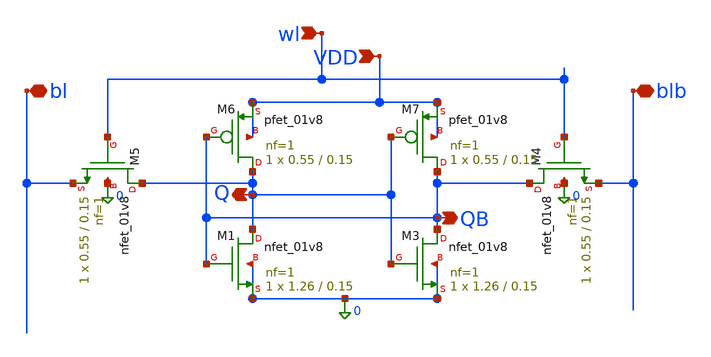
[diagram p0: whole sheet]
** sch_path: xschem/Subcircuits/six_t.sch
**.subckt six_t bl Q QB wl VDD blb
*.iopin bl
*.opin Q
*.opin QB
*.ipin wl
*.ipin VDD
*.iopin blb
XM3 QB Q 0 0 sky130_fd_pr__nfet_01v8 L=0.15 W=1.26 nf=1 ad='int((nf+1)/2) * W/nf * 0.29' as='int((nf+2)/2) * W/nf * 0.29'
+ pd='2*int((nf+1)/2) * (W/nf + 0.29)' ps='2*int((nf+2)/2) * (W/nf + 0.29)' nrd='0.29 / W' nrs='0.29 / W'
+ sa=0 sb=0 sd=0 mult=1 m=1
XM4 QB wl blb 0 sky130_fd_pr__nfet_01v8 L=0.15 W=0.55 nf=1 ad='int((nf+1)/2) * W/nf * 0.29' as='int((nf+2)/2) * W/nf * 0.29'
+ pd='2*int((nf+1)/2) * (W/nf + 0.29)' ps='2*int((nf+2)/2) * (W/nf + 0.29)' nrd='0.29 / W' nrs='0.29 / W'
+ sa=0 sb=0 sd=0 mult=1 m=1
XM5 Q wl bl 0 sky130_fd_pr__nfet_01v8 L=0.15 W=0.55 nf=1 ad='int((nf+1)/2) * W/nf * 0.29' as='int((nf+2)/2) * W/nf * 0.29'
+ pd='2*int((nf+1)/2) * (W/nf + 0.29)' ps='2*int((nf+2)/2) * (W/nf + 0.29)' nrd='0.29 / W' nrs='0.29 / W'
+ sa=0 sb=0 sd=0 mult=1 m=1
XM6 Q QB VDD VDD sky130_fd_pr__pfet_01v8 L=0.15 W=0.55 nf=1 ad='int((nf+1)/2) * W/nf * 0.29' as='int((nf+2)/2) * W/nf * 0.29'
+ pd='2*int((nf+1)/2) * (W/nf + 0.29)' ps='2*int((nf+2)/2) * (W/nf + 0.29)' nrd='0.29 / W' nrs='0.29 / W'
+ sa=0 sb=0 sd=0 mult=1 m=1
XM7 QB Q VDD VDD sky130_fd_pr__pfet_01v8 L=0.15 W=0.55 nf=1 ad='int((nf+1)/2) * W/nf * 0.29' as='int((nf+2)/2) * W/nf * 0.29'
+ pd='2*int((nf+1)/2) * (W/nf + 0.29)' ps='2*int((nf+2)/2) * (W/nf + 0.29)' nrd='0.29 / W' nrs='0.29 / W'
+ sa=0 sb=0 sd=0 mult=1 m=1
XM1 Q QB 0 0 sky130_fd_pr__nfet_01v8 L=0.15 W=1.26 nf=1 ad='int((nf+1)/2) * W/nf * 0.29' as='int((nf+2)/2) * W/nf * 0.29'
+ pd='2*int((nf+1)/2) * (W/nf + 0.29)' ps='2*int((nf+2)/2) * (W/nf + 0.29)' nrd='0.29 / W' nrs='0.29 / W'
+ sa=0 sb=0 sd=0 mult=1 m=1
**** begin user architecture code


.lib /home/kaavya/.ciel/ciel/sky130/versions/9233c19260cd813c3fa67dd4594fe4cc67016832/sky130A/libs.tech/ngspice/sky130.lib.spice tt

VDD VDD 0 1.8
.ic v(Q)=1.8 v(QB)=0

Vbl bl 0 0
Vblb blb 0 1.8
Vwl wl 0 PULSE(0 1.8 2n 10p 10p 3n 10n)

.tran 10p 10n
.control
run
plot v(wl)+4 v(Q)+2 v(QB)
.endc
.save all


**** end user architecture code
**.ends
.end
